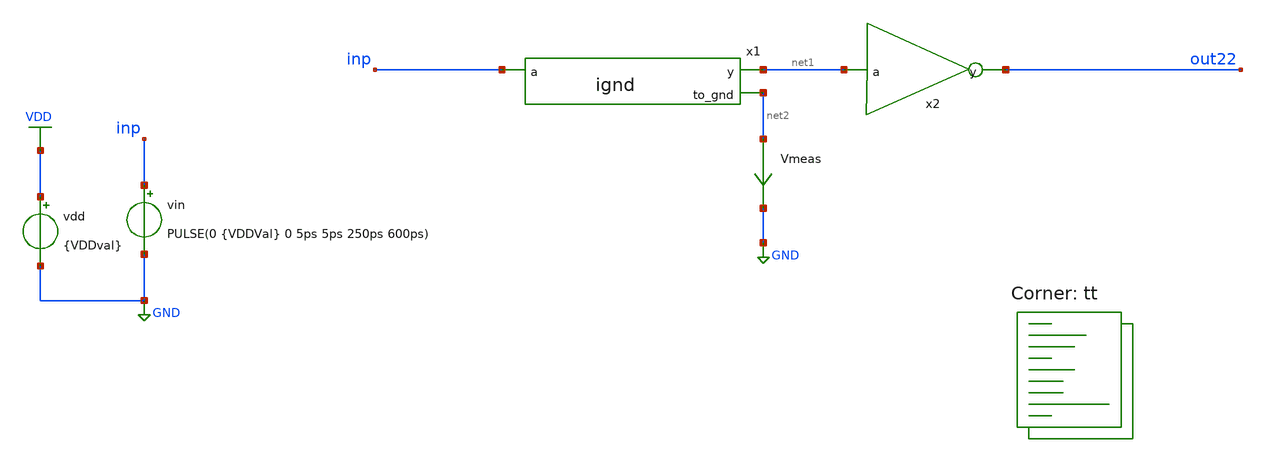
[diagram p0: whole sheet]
** sch_path: assignments/assignment3/assign1b.sch
**.subckt assign1b
vin inp GND PULSE(0 {VDDVal} 0 5ps 5ps 250ps 600ps)
x1 net1 inp net2 ignd
x2 out22 net1 inverter
Vmeas net2 GND 0
.save i(vmeas)
vdd VDD GND {VDDval}
**** begin user architecture code


.param VDDVal = 1.8
.param width_p = 0.84

.save all

.control
let Nsim = 9
let delayvec = vector(Nsim)
let delayvec_ana = vector(Nsim)
let vddvec = vector(Nsim)
let index = 0

* Analytical Constants
let Ctot = 3.8e-15
let Vtn = 0.7
let Vtp = 0.7
let EcnLn = 0.96
let EcpLp = 1.0
let Kn_WL = 5.838e-4
let Kp_WL = 4.112e-4

while index < Nsim
  let vddv = 1.0 + (index * 0.1)
  let vby2 = vddv / 2

  alterparam VDDVal = $&vddv
  reset
  tran 1p 600p

  * 1. SIMULATED DELAY (SPICE)
  meas tran thl trig v(inp) val=$&vby2 rise=1 targ v(net1) val=$&vby2 fall=1
  meas tran tlh trig v(inp) val=$&vby2 fall=1 targ v(net1) val=$&vby2 rise=1
  let delayvec[index] = (thl + tlh) / 2

  * 2. ANALYTICAL DELAY (Velocity Saturation Model)
  let num_hl = Ctot * vby2 * (EcnLn + vddv - Vtn)
  let den_hl = Kn_WL * EcnLn * (vddv - Vtn) * (vddv - Vtn)
  let tphl_ana = num_hl / den_hl

  let num_lh = Ctot * vby2 * (EcpLp + vddv - Vtp)
  let den_lh = Kp_WL * EcpLp * (vddv - Vtp) * (vddv - Vtp)
  let tplh_ana = num_lh / den_lh

  let delayvec_ana[index] = (tphl_ana + tplh_ana) / 2

  * 3. LOG X-AXIS
  let vddvec[index] = vddv
  let index = index + 1
end

* Plot both the Simulated (delayvec) and Analytical (delayvec_ana) curves
plot delayvec delayvec_ana vs vddvec
.endc


.lib $::SKYWATER_MODELS/sky130.lib.spice tt
**** end user architecture code
**.ends
.GLOBAL GND
.GLOBAL VDD
.end
